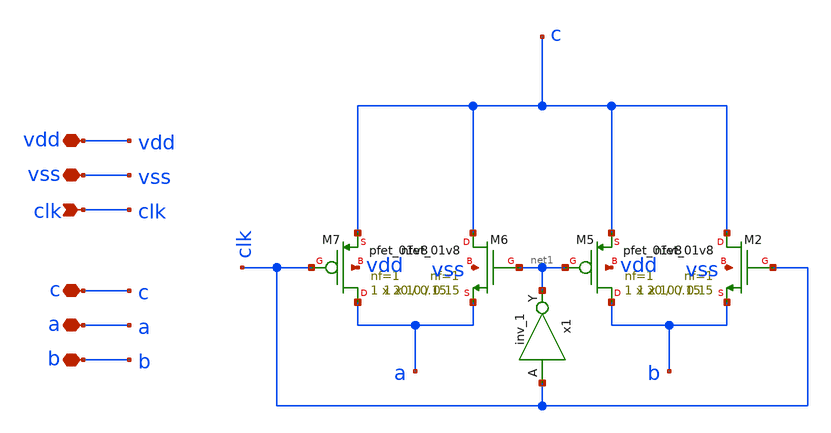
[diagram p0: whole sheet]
** sch_path: xschem/dac/dac_sw.sch
**.subckt dac_sw vdd vss clk c a b
*.iopin vdd
*.iopin vss
*.ipin clk
*.iopin c
*.iopin a
*.iopin b
XM2 c clk b vss sky130_fd_pr__nfet_01v8 L=0.15 W=10 nf=1 ad='int((nf+1)/2) * W/nf * 0.29' as='int((nf+2)/2) * W/nf * 0.29'
+ pd='2*int((nf+1)/2) * (W/nf + 0.29)' ps='2*int((nf+2)/2) * (W/nf + 0.29)' nrd='0.29 / W' nrs='0.29 / W'
+ sa=0 sb=0 sd=0 mult=1 m=1
XM5 b net1 c vdd sky130_fd_pr__pfet_01v8 L=0.15 W=20 nf=1 ad='int((nf+1)/2) * W/nf * 0.29' as='int((nf+2)/2) * W/nf * 0.29'
+ pd='2*int((nf+1)/2) * (W/nf + 0.29)' ps='2*int((nf+2)/2) * (W/nf + 0.29)' nrd='0.29 / W' nrs='0.29 / W'
+ sa=0 sb=0 sd=0 mult=1 m=1
XM6 c net1 a vss sky130_fd_pr__nfet_01v8 L=0.15 W=10 nf=1 ad='int((nf+1)/2) * W/nf * 0.29' as='int((nf+2)/2) * W/nf * 0.29'
+ pd='2*int((nf+1)/2) * (W/nf + 0.29)' ps='2*int((nf+2)/2) * (W/nf + 0.29)' nrd='0.29 / W' nrs='0.29 / W'
+ sa=0 sb=0 sd=0 mult=1 m=1
XM7 a clk c vdd sky130_fd_pr__pfet_01v8 L=0.15 W=20 nf=1 ad='int((nf+1)/2) * W/nf * 0.29' as='int((nf+2)/2) * W/nf * 0.29'
+ pd='2*int((nf+1)/2) * (W/nf + 0.29)' ps='2*int((nf+2)/2) * (W/nf + 0.29)' nrd='0.29 / W' nrs='0.29 / W'
+ sa=0 sb=0 sd=0 mult=1 m=1
x1 clk vss vss vdd vdd net1 sky130_fd_sc_hd__inv_1
**.ends
.end
